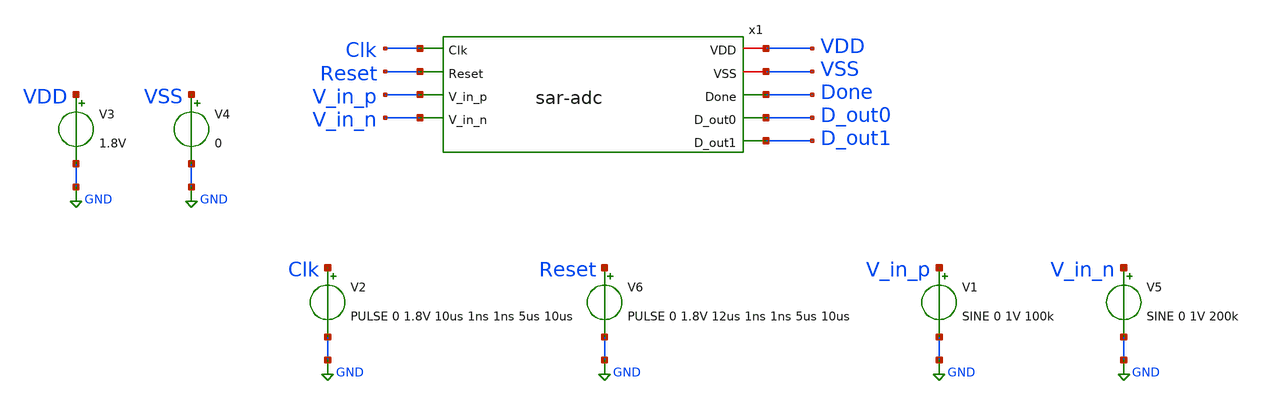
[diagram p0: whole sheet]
** sch_path: xschem/tests/sar-adc/sar-adc_test.sch
**.subckt sar-adc_test
V3 VDD GND 1.8V
V4 VSS GND 0
x1 VDD VSS Clk Reset V_in_p V_in_n Done D_out0 D_out1 sar-adc
V2 Clk GND PULSE 0 1.8V 10us 1ns 1ns 5us 10us
V1 V_in_p GND SINE 0 1V 100k
V5 V_in_n GND SINE 0 1V 200k
V6 Reset GND PULSE 0 1.8V 12us 1ns 1ns 5us 10us
**** begin user architecture code
 .lib $::SKYWATER_MODELS/sky130.lib.spice tt
.include $::SKYWATER_STDCELLS/sky130_fd_sc_hd.spice


.options acct list
.temp 25
*vvcc VDD 0 dc 1.8
*vvss VSS 0 0
.control
tran 0.1u 100u
plot Clk Reset+2 Done+4
plot V_in_p D_out0 V_in_n+2 D_out1+2
write sar-adc_test.raw
.endc


**** end user architecture code
**.ends

* expanding   symbol:  src/sar-adc/sar-adc.sym # of pins=9
** sym_path: xschem/src/sar-adc/sar-adc.sym
** sch_path: xschem/src/sar-adc/sar-adc.sch
.subckt sar-adc VDD VSS Clk Reset V_in_p V_in_n Done D_out0 D_out1
*.iopin VDD
*.ipin V_in_p
*.opin Done
*.iopin VSS
*.ipin V_in_n
*.ipin Reset
*.opin D_out0
*.opin D_out1
*.ipin Clk
R1 VSS D_out0 sky130_fd_pr__res_generic_m1 W=1 L=1 m=1
R2 D_out0 V_in_p sky130_fd_pr__res_generic_m1 W=1 L=1 m=1
R3 VSS D_out1 sky130_fd_pr__res_generic_m1 W=1 L=1 m=1
R4 D_out1 V_in_n sky130_fd_pr__res_generic_m1 W=1 L=1 m=1
x2 Clk Reset VSS VSS VDD VDD Done sky130_fd_sc_hd__and2_0
.ends

.GLOBAL GND
.end
